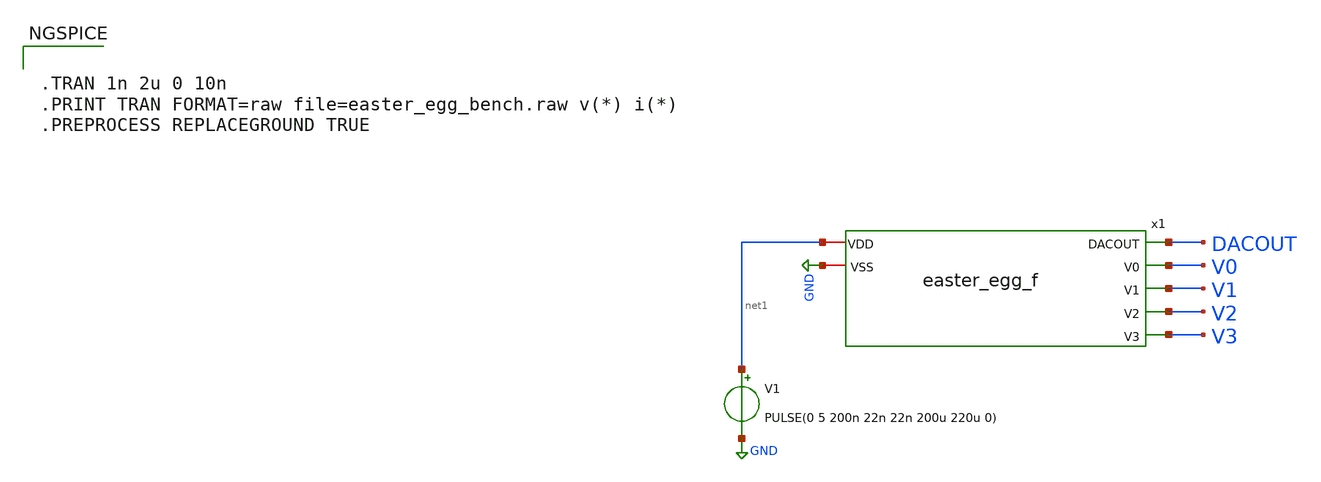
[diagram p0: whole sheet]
** sch_path: analog/xschem/easter_egg_bench.sch
**.subckt easter_egg_bench
x1 net1 GND DACOUT V0 V1 V2 V3 easter_egg_f
V1 net1 GND PULSE(0 5 200n 22n 22n 200u 220u 0)
**** begin user architecture code


.TRAN 1n 2u 0 10n
.PRINT TRAN FORMAT=raw file=easter_egg_bench.raw v(*) i(*)
.PREPROCESS REPLACEGROUND TRUE



.include /run/media/veracrypt1/ws-charge-controller/analog/xschem/extracted/easter_egg_f.spice
.include $::PDK_ROOT/gf180mcuD/libs.tech/xyce/design.xyce
.lib $::PDK_ROOT/gf180mcuD/libs.tech/xyce/sm141064.xyce typical
.lib $::PDK_ROOT/gf180mcuD/libs.tech/xyce/sm141064.xyce res_typical
.lib $::PDK_ROOT/gf180mcuD/libs.tech/xyce/sm141064.xyce diode_typical
.lib $::PDK_ROOT/gf180mcuD/libs.tech/xyce/sm141064.xyce mimcap_typical
.lib $::PDK_ROOT/gf180mcuD/libs.tech/xyce/sm141064.xyce cap_mim

**** end user architecture code
**.ends
.GLOBAL GND
.end
